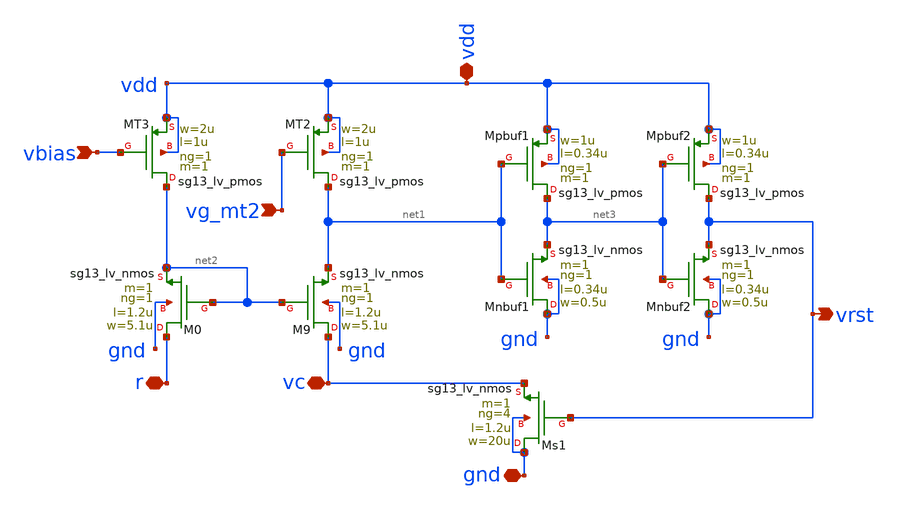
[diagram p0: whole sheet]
** sch_path: Enfoque_B/xschem/celdas/osc_relax.sch
**.subckt osc_relax vc r vdd gnd vbias vg_mt2 vrst
*.iopin vc
*.iopin r
*.iopin vdd
*.iopin gnd
*.ipin vbias
*.ipin vg_mt2
*.opin vrst
XMT3 net2 vbias vdd vdd sg13_lv_pmos w=2u l=1u ng=1 m=1 mm_ok=1
XMT2 net1 vg_mt2 vdd vdd sg13_lv_pmos w=2u l=1u ng=1 m=1 mm_ok=1
XM9 vc net2 net1 gnd sg13_lv_nmos w=5.1u l=1.2u ng=1 m=1 mm_ok=1
XM0 r net2 net2 gnd sg13_lv_nmos w=5.1u l=1.2u ng=1 m=1 mm_ok=1
XMpbuf2 vrst net3 vdd vdd sg13_lv_pmos w=1u l=0.34u ng=1 m=1 mm_ok=1
XMnbuf1 gnd net1 net3 gnd sg13_lv_nmos w=0.5u l=0.34u ng=1 m=1 mm_ok=1
XMnbuf2 gnd net3 vrst gnd sg13_lv_nmos w=0.5u l=0.34u ng=1 m=1 mm_ok=1
XMs1 gnd vrst vc gnd sg13_lv_nmos w=20u l=1.2u ng=4 m=1 mm_ok=1
XMpbuf1 net3 net1 vdd vdd sg13_lv_pmos w=1u l=0.34u ng=1 m=1 mm_ok=1
**.ends
.end
